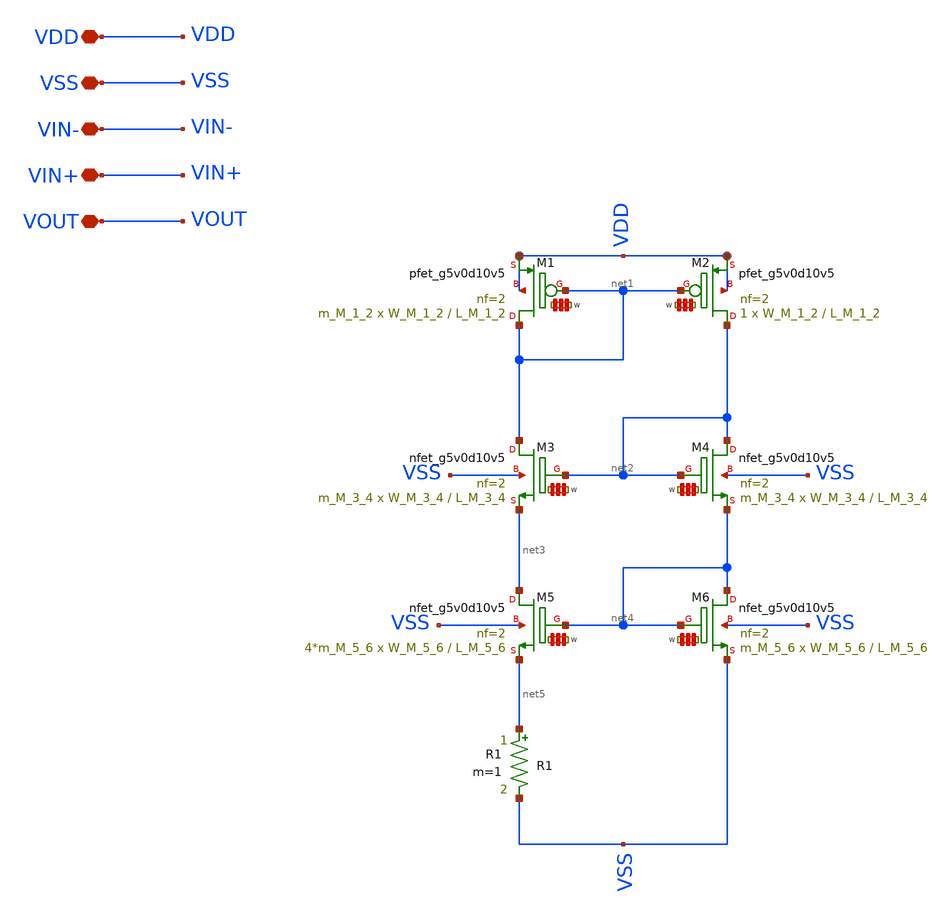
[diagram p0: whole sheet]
** sch_path: automatization_analog_design/transimpedance_amplifier_with_two_stage/opamp/opamp.sch
**.subckt opamp VDD VSS VIN- VIN+ VOUT
*.iopin VDD
*.iopin VSS
*.iopin VIN-
*.iopin VIN+
*.iopin VOUT
XM2 net2 net1 VDD VDD sky130_fd_pr__pfet_g5v0d10v5 L=L_M_1_2 W='W_M_1_2 * 2 ' nf=2 ad='int((2 + 1)/2) * W_M_1_2 * 0.29'
+ as='int((2 + 2)/2) * W_M_1_2 * 0.29' pd='2*int((2 + 1)/2) * (W_M_1_2 + 0.29)' ps='2*int((2 + 2)/2) * (W_M_1_2 + 0.29)'
+ nrd='0.29 / W_M_1_2 / 2 ' nrs='0.29 / W_M_1_2 / 2 ' sa=0 sb=0 sd=0 mult=1 m=1
XM1 net1 net1 VDD VDD sky130_fd_pr__pfet_g5v0d10v5 L=L_M_1_2 W='W_M_1_2 * 2 ' nf=2 ad='int((2 + 1)/2) * W_M_1_2 * 0.29'
+ as='int((2 + 2)/2) * W_M_1_2 * 0.29' pd='2*int((2 + 1)/2) * (W_M_1_2 + 0.29)' ps='2*int((2 + 2)/2) * (W_M_1_2 + 0.29)'
+ nrd='0.29 / W_M_1_2 / 2 ' nrs='0.29 / W_M_1_2 / 2 ' sa=0 sb=0 sd=0 mult=m_M_1_2 m=m_M_1_2
XM4 net2 net2 net4 VSS sky130_fd_pr__nfet_g5v0d10v5 L=L_M_3_4 W='W_M_3_4 * 2 ' nf=2 ad='int((nf+1)/2) * W / nf * 0.29'
+ as='int((nf+2)/2) * W / nf * 0.29' pd='2*int((nf+1)/2) * (W / nf + 0.29)' ps='2*int((nf+2)/2) * (W / nf + 0.29)'
+ nrd='0.29 / W ' nrs='0.29 / W ' sa=0 sb=0 sd=0 mult=m_M_3_4 m=m_M_3_4
XM3 net1 net2 net3 VSS sky130_fd_pr__nfet_g5v0d10v5 L=L_M_3_4 W='W_M_3_4 * 2 ' nf=2 ad='int((nf+1)/2) * W / nf * 0.29'
+ as='int((nf+2)/2) * W / nf * 0.29' pd='2*int((nf+1)/2) * (W / nf + 0.29)' ps='2*int((nf+2)/2) * (W / nf + 0.29)'
+ nrd='0.29 / W ' nrs='0.29 / W ' sa=0 sb=0 sd=0 mult=m_M_3_4 m=m_M_3_4
XM5 net3 net4 net5 VSS sky130_fd_pr__nfet_g5v0d10v5 L=L_M_5_6 W='W_M_5_6 * 2 ' nf=2 ad='int((nf+1)/2) * W / nf * 0.29'
+ as='int((nf+2)/2) * W / nf * 0.29' pd='2*int((nf+1)/2) * (W / nf + 0.29)' ps='2*int((nf+2)/2) * (W / nf + 0.29)'
+ nrd='0.29 / W ' nrs='0.29 / W ' sa=0 sb=0 sd=0 mult=4*m_M_5_6 m=4*m_M_5_6
XM6 net4 net4 VSS VSS sky130_fd_pr__nfet_g5v0d10v5 L=L_M_5_6 W='W_M_5_6 * 2 ' nf=2 ad='int((nf+1)/2) * W / nf * 0.29'
+ as='int((nf+2)/2) * W / nf * 0.29' pd='2*int((nf+1)/2) * (W / nf + 0.29)' ps='2*int((nf+2)/2) * (W / nf + 0.29)'
+ nrd='0.29 / W ' nrs='0.29 / W ' sa=0 sb=0 sd=0 mult=m_M_5_6 m=m_M_5_6
R1 net5 VSS R1 m=1
**.ends
.end
